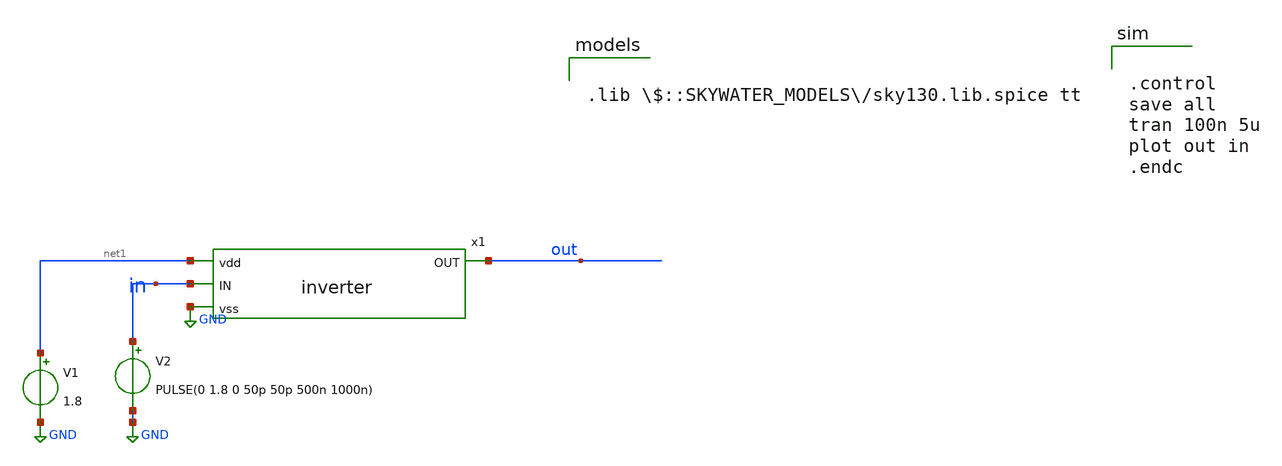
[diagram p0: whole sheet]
** sch_path: inverter_test.sch
**.subckt inverter_test
x1 net1 out in GND inverter
V1 net1 GND 1.8
V2 in GND PULSE(0 1.8 0 50p 50p 500n 1000n)
**** begin user architecture code

.lib $::SKYWATER_MODELS/sky130.lib.spice tt



.control
save all
tran 100n 5u
plot out in
.endc


**** end user architecture code
**.ends

* expanding   symbol:  /home/kuba/project/xschem_inv/inverter.sym # of pins=4
** sym_path: inverter.sym
** sch_path: inverter.sch
.subckt inverter vdd OUT IN vss
*.opin OUT
*.ipin IN
*.ipin vdd
*.ipin vss
XM1 OUT IN vss vss sky130_fd_pr__nfet_01v8 L=0.15 W=1 nf=1 ad='int((nf+1)/2) * W/nf * 0.29' as='int((nf+2)/2) * W/nf * 0.29'
+ pd='2*int((nf+1)/2) * (W/nf + 0.29)' ps='2*int((nf+2)/2) * (W/nf + 0.29)' nrd='0.29 / W' nrs='0.29 / W'
+ sa=0 sb=0 sd=0 mult=1 m=1
XM2 OUT IN vdd VDD sky130_fd_pr__pfet_01v8 L=0.15 W=1 nf=1 ad='int((nf+1)/2) * W/nf * 0.29' as='int((nf+2)/2) * W/nf * 0.29'
+ pd='2*int((nf+1)/2) * (W/nf + 0.29)' ps='2*int((nf+2)/2) * (W/nf + 0.29)' nrd='0.29 / W' nrs='0.29 / W'
+ sa=0 sb=0 sd=0 mult=2 m=2
.ends

.GLOBAL GND
.end
